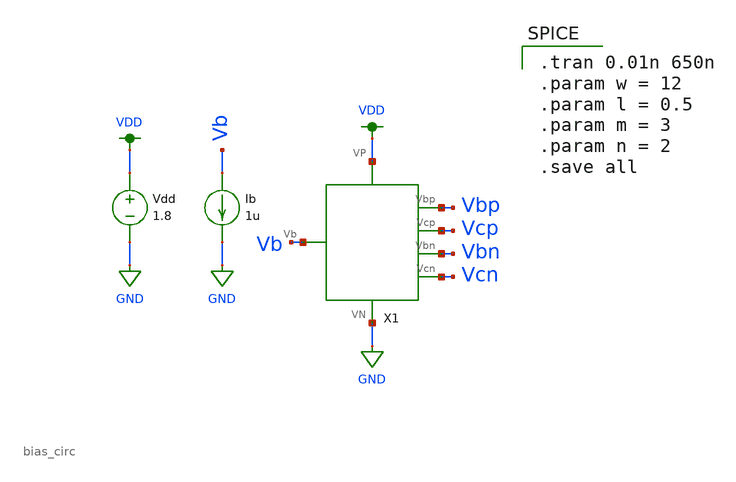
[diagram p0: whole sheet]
** sch_path: Mini_Project_3/bias_circ_vienna/bias_circ_sim.sch
**.subckt bias_circ_sim
X1 VDD GND Vcn Vbn Vcp Vbp Vb bias_circ
Vdd VDD GND 1.8
Ib Vb GND 1u
**** begin user architecture code

.tran 0.01n 650n
.param w = 12
.param l = 0.5
.param m = 3
.param n = 2
.save all


.option wnflag=1
.lib ~/skywater/skywater-pdk/libraries/sky130_fd_pr_ngspice/latest/models/sky130.lib.spice tt

**** end user architecture code
**.ends

* expanding   symbol:  /home/vscheyer/MADVLSI/Mini_Project_3/bias_circ.sym # of pins=7
** sym_path: Mini_Project_3/bias_circ.sym
** sch_path: Mini_Project_3/bias_circ.sch
.subckt bias_circ VP VN Vcn Vbn Vcp Vbp Vb
*.iopin VP
*.iopin VN
*.iopin VP
*.iopin Vcn
*.iopin Vb
*.iopin VP
*.iopin VP
*.iopin Vbp
*.iopin Vbn
*.iopin VN
*.iopin VN
*.iopin Vcp
*.iopin VN
*.iopin VP
XM3 net1 Vbp VP VDD sky130_fd_pr__pfet_01v8 L=l W=w nf=1 ad='int((nf+1)/2) * W/nf * 0.29' as='int((nf+2)/2) * W/nf * 0.29'
+ pd='2*int((nf+1)/2) * (W/nf + 0.29)' ps='2*int((nf+2)/2) * (W/nf + 0.29)' nrd='0.29 / W' nrs='0.29 / W'
+ sa=0 sb=0 sd=0 mult=1 m=1
XM4 VP Vbp Vb VDD sky130_fd_pr__pfet_01v8 L=l W=w nf=1 ad='int((nf+1)/2) * W/nf * 0.29' as='int((nf+2)/2) * W/nf * 0.29'
+ pd='2*int((nf+1)/2) * (W/nf + 0.29)' ps='2*int((nf+2)/2) * (W/nf + 0.29)' nrd='0.29 / W' nrs='0.29 / W'
+ sa=0 sb=0 sd=0 mult=1 m=1
XM6 Vcn Vbp VP VDD sky130_fd_pr__pfet_01v8 L=l W=w nf=1 ad='int((nf+1)/2) * W/nf * 0.29' as='int((nf+2)/2) * W/nf * 0.29'
+ pd='2*int((nf+1)/2) * (W/nf + 0.29)' ps='2*int((nf+2)/2) * (W/nf + 0.29)' nrd='0.29 / W' nrs='0.29 / W'
+ sa=0 sb=0 sd=0 mult=1 m=1
XM1 net1 net1 net2 GND sky130_fd_pr__nfet_01v8 L=l W=m nf=1 ad='int((nf+1)/2) * W/nf * 0.29' as='int((nf+2)/2) * W/nf * 0.29'
+ pd='2*int((nf+1)/2) * (W/nf + 0.29)' ps='2*int((nf+2)/2) * (W/nf + 0.29)' nrd='0.29 / W' nrs='0.29 / W'
+ sa=0 sb=0 sd=0 mult=1 m=1
XM2 net2 Vcn Vcn GND sky130_fd_pr__nfet_01v8 L=l W=w nf=1 ad='int((nf+1)/2) * W/nf * 0.29' as='int((nf+2)/2) * W/nf * 0.29'
+ pd='2*int((nf+1)/2) * (W/nf + 0.29)' ps='2*int((nf+2)/2) * (W/nf + 0.29)' nrd='0.29 / W' nrs='0.29 / W'
+ sa=0 sb=0 sd=0 mult=1 m=1
XM5 net2 net1 VN GND sky130_fd_pr__nfet_01v8 L=l W=w nf=1 ad='int((nf+1)/2) * W/nf * 0.29' as='int((nf+2)/2) * W/nf * 0.29'
+ pd='2*int((nf+1)/2) * (W/nf + 0.29)' ps='2*int((nf+2)/2) * (W/nf + 0.29)' nrd='0.29 / W' nrs='0.29 / W'
+ sa=0 sb=0 sd=0 mult=1 m=1
XM7 net3 Vbp VP VDD sky130_fd_pr__pfet_01v8 L=l W=w nf=1 ad='int((nf+1)/2) * W/nf * 0.29' as='int((nf+2)/2) * W/nf * 0.29'
+ pd='2*int((nf+1)/2) * (W/nf + 0.29)' ps='2*int((nf+2)/2) * (W/nf + 0.29)' nrd='0.29 / W' nrs='0.29 / W'
+ sa=0 sb=0 sd=0 mult=1 m=1
XM8 net3 Vbn VN GND sky130_fd_pr__nfet_01v8 L=l W=w nf=1 ad='int((nf+1)/2) * W/nf * 0.29' as='int((nf+2)/2) * W/nf * 0.29'
+ pd='2*int((nf+1)/2) * (W/nf + 0.29)' ps='2*int((nf+2)/2) * (W/nf + 0.29)' nrd='0.29 / W' nrs='0.29 / W'
+ sa=0 sb=0 sd=0 mult=1 m=1
XM9 Vcp Vbn VN GND sky130_fd_pr__nfet_01v8 L=l W=w nf=1 ad='int((nf+1)/2) * W/nf * 0.29' as='int((nf+2)/2) * W/nf * 0.29'
+ pd='2*int((nf+1)/2) * (W/nf + 0.29)' ps='2*int((nf+2)/2) * (W/nf + 0.29)' nrd='0.29 / W' nrs='0.29 / W'
+ sa=0 sb=0 sd=0 mult=1 m=1
XM10 net4 Vbn VN GND sky130_fd_pr__nfet_01v8 L=l W=w nf=1 ad='int((nf+1)/2) * W/nf * 0.29' as='int((nf+2)/2) * W/nf * 0.29'
+ pd='2*int((nf+1)/2) * (W/nf + 0.29)' ps='2*int((nf+2)/2) * (W/nf + 0.29)' nrd='0.29 / W' nrs='0.29 / W'
+ sa=0 sb=0 sd=0 mult=1 m=1
XM11 Vcp Vcp net5 VDD sky130_fd_pr__pfet_01v8 L=l W=w nf=1 ad='int((nf+1)/2) * W/nf * 0.29' as='int((nf+2)/2) * W/nf * 0.29'
+ pd='2*int((nf+1)/2) * (W/nf + 0.29)' ps='2*int((nf+2)/2) * (W/nf + 0.29)' nrd='0.29 / W' nrs='0.29 / W'
+ sa=0 sb=0 sd=0 mult=1 m=1
XM12 net5 net4 net4 VDD sky130_fd_pr__pfet_01v8 L=l W=m nf=1 ad='int((nf+1)/2) * W/nf * 0.29' as='int((nf+2)/2) * W/nf * 0.29'
+ pd='2*int((nf+1)/2) * (W/nf + 0.29)' ps='2*int((nf+2)/2) * (W/nf + 0.29)' nrd='0.29 / W' nrs='0.29 / W'
+ sa=0 sb=0 sd=0 mult=1 m=1
XM13 VP net4 net5 VDD sky130_fd_pr__pfet_01v8 L=l W=w nf=1 ad='int((nf+1)/2) * W/nf * 0.29' as='int((nf+2)/2) * W/nf * 0.29'
+ pd='2*int((nf+1)/2) * (W/nf + 0.29)' ps='2*int((nf+2)/2) * (W/nf + 0.29)' nrd='0.29 / W' nrs='0.29 / W'
+ sa=0 sb=0 sd=0 mult=1 m=1
.ends

.GLOBAL VDD
.GLOBAL GND
.end
